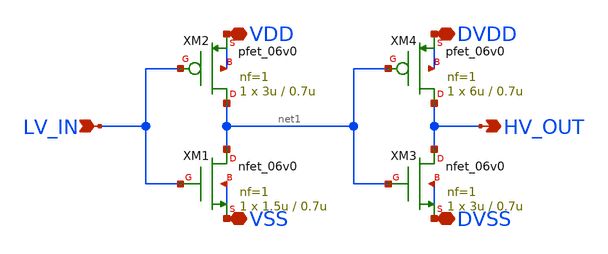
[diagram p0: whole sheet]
** sch_path: shifters/basic_shifter_lh.sch
**.subckt basic_shifter_lh LV_IN HV_OUT DVDD DVSS VDD VSS
*.ipin LV_IN
*.opin HV_OUT
*.iopin DVDD
*.iopin DVSS
*.iopin VDD
*.iopin VSS
XM1 net1 LV_IN VSS VSS nfet_06v0 L=0.7u W=1.5u nf=1 ad='int((nf+1)/2) * W/nf * 0.18u' as='int((nf+2)/2) * W/nf * 0.18u'
+ pd='2*int((nf+1)/2) * (W/nf + 0.18u)' ps='2*int((nf+2)/2) * (W/nf + 0.18u)' nrd='0.18u / W' nrs='0.18u / W'
+ sa=0 sb=0 sd=0 m=1
XM2 net1 LV_IN VDD VDD pfet_06v0 L=0.7u W=3u nf=1 ad='int((nf+1)/2) * W/nf * 0.18u' as='int((nf+2)/2) * W/nf * 0.18u'
+ pd='2*int((nf+1)/2) * (W/nf + 0.18u)' ps='2*int((nf+2)/2) * (W/nf + 0.18u)' nrd='0.18u / W' nrs='0.18u / W'
+ sa=0 sb=0 sd=0 m=1
XM3 HV_OUT net1 DVSS DVSS nfet_06v0 L=0.7u W=3u nf=1 ad='int((nf+1)/2) * W/nf * 0.18u' as='int((nf+2)/2) * W/nf * 0.18u'
+ pd='2*int((nf+1)/2) * (W/nf + 0.18u)' ps='2*int((nf+2)/2) * (W/nf + 0.18u)' nrd='0.18u / W' nrs='0.18u / W'
+ sa=0 sb=0 sd=0 m=1
XM4 HV_OUT net1 DVDD DVDD pfet_06v0 L=0.7u W=6u nf=1 ad='int((nf+1)/2) * W/nf * 0.18u' as='int((nf+2)/2) * W/nf * 0.18u'
+ pd='2*int((nf+1)/2) * (W/nf + 0.18u)' ps='2*int((nf+2)/2) * (W/nf + 0.18u)' nrd='0.18u / W' nrs='0.18u / W'
+ sa=0 sb=0 sd=0 m=1
**.ends
.end
